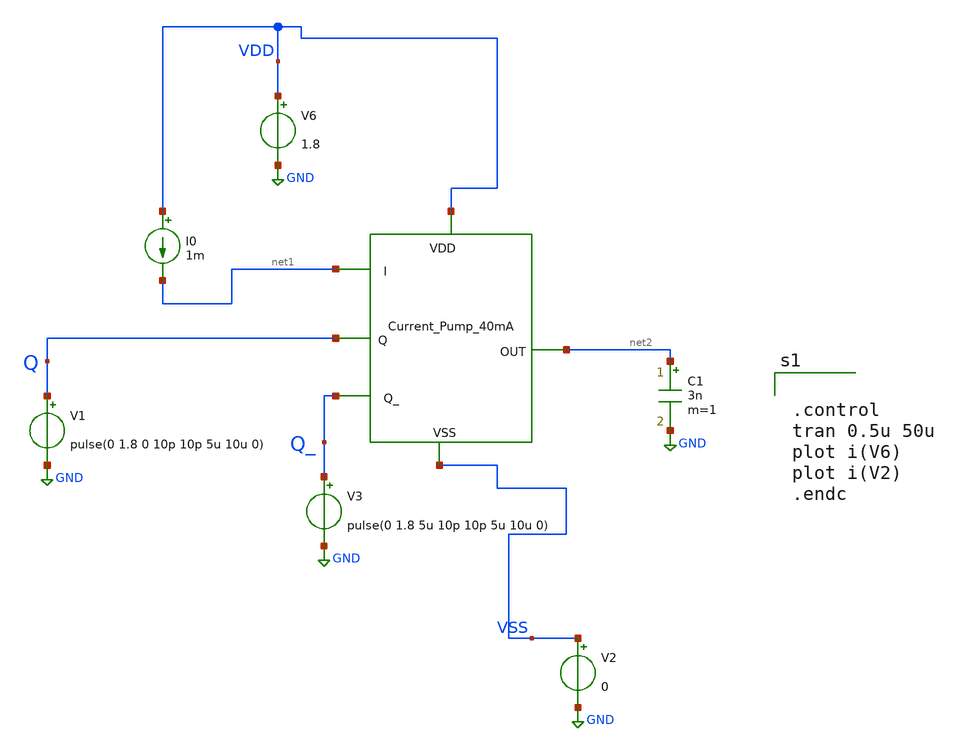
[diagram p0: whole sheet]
** sch_path: xschem/DC_DC_Converter_xschem/OTHERS/DC_DC_Converter_JV11/Current_pump_mirror/Current_pump_40mA_tb.sch
**.subckt Current_pump_40mA_tb
V1 Q GND pulse(0 1.8 0 10p 10p 5u 10u 0)
V3 Q_ GND pulse(0 1.8 5u 10p 10p 5u 10u 0)
I0 VDD net1 1m
C1 net2 GND 3n m=1
V6 VDD GND 1.8
V2 VSS GND 0
x1 net1 VDD VSS Q Q_ net2 Current_pump_40mA
**** begin user architecture code


.control
tran 0.5u 50u
plot i(V6)
plot i(V2)
.endc



** opencircuitdesign pdks install
.lib $::SKYWATER_MODELS/sky130.lib.spice tt


**** end user architecture code
**.ends
.GLOBAL GND
.end
